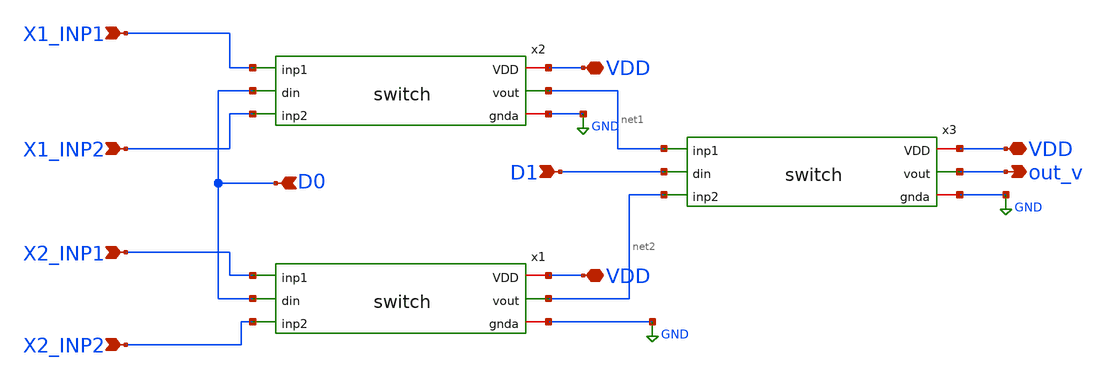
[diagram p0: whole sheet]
** sch_path: week7/pre-layout/untitled-3.sch
**.subckt untitled-3 out_v VDD VDD VDD X1_INP1 X1_INP2 X2_INP1 X2_INP2 D0 D1
*.opin out_v
*.iopin VDD
*.iopin VDD
*.iopin VDD
*.ipin X1_INP1
*.ipin X1_INP2
*.ipin X2_INP1
*.ipin X2_INP2
*.ipin D0
*.ipin D1
x1 X2_INP1 VDD D0 net2 GND X2_INP2 switch
x2 X1_INP1 VDD D0 net1 GND X1_INP2 switch
x3 net1 VDD D1 out_v GND net2 switch
**.ends

* expanding   symbol:  switch.sym # of pins=6
** sym_path: week7/pre-layout/switch.sym
** sch_path: week7/pre-layout/switch.sch
.subckt switch inp1 VDD din vout gnda inp2
*.ipin din
*.iopin VDD
*.ipin inp1
*.ipin inp2
*.iopin gnda
*.opin vout
XM1 net1 din gnda gnda sky130_fd_pr__nfet_01v8 L=0.15 W=0.6 nf=1 ad='int((nf+1)/2) * W/nf * 0.29' as='int((nf+2)/2) * W/nf * 0.29'
+ pd='2*int((nf+1)/2) * (W/nf + 0.29)' ps='2*int((nf+2)/2) * (W/nf + 0.29)' nrd='0.29 / W' nrs='0.29 / W'
+ sa=0 sb=0 sd=0 mult=1 m=1
XM2 net1 din VDD VDD sky130_fd_pr__pfet_01v8 L=0.15 W=1.2 nf=1 ad='int((nf+1)/2) * W/nf * 0.29' as='int((nf+2)/2) * W/nf * 0.29'
+ pd='2*int((nf+1)/2) * (W/nf + 0.29)' ps='2*int((nf+2)/2) * (W/nf + 0.29)' nrd='0.29 / W' nrs='0.29 / W'
+ sa=0 sb=0 sd=0 mult=1 m=1
XM3 net2 net1 VDD VDD sky130_fd_pr__pfet_01v8 L=0.15 W=1.2 nf=1 ad='int((nf+1)/2) * W/nf * 0.29' as='int((nf+2)/2) * W/nf * 0.29'
+ pd='2*int((nf+1)/2) * (W/nf + 0.29)' ps='2*int((nf+2)/2) * (W/nf + 0.29)' nrd='0.29 / W' nrs='0.29 / W'
+ sa=0 sb=0 sd=0 mult=1 m=1
XM4 net2 net1 gnda gnda sky130_fd_pr__nfet_01v8 L=0.15 W=0.6 nf=1 ad='int((nf+1)/2) * W/nf * 0.29' as='int((nf+2)/2) * W/nf * 0.29'
+ pd='2*int((nf+1)/2) * (W/nf + 0.29)' ps='2*int((nf+2)/2) * (W/nf + 0.29)' nrd='0.29 / W' nrs='0.29 / W'
+ sa=0 sb=0 sd=0 mult=1 m=1
XM5 inp2 net2 vout VDD sky130_fd_pr__pfet_01v8 L=0.15 W=1.2 nf=1 ad='int((nf+1)/2) * W/nf * 0.29' as='int((nf+2)/2) * W/nf * 0.29'
+ pd='2*int((nf+1)/2) * (W/nf + 0.29)' ps='2*int((nf+2)/2) * (W/nf + 0.29)' nrd='0.29 / W' nrs='0.29 / W'
+ sa=0 sb=0 sd=0 mult=1 m=1
XM6 inp1 net2 vout GND sky130_fd_pr__nfet_01v8 L=0.15 W=0.6 nf=1 ad='int((nf+1)/2) * W/nf * 0.29' as='int((nf+2)/2) * W/nf * 0.29'
+ pd='2*int((nf+1)/2) * (W/nf + 0.29)' ps='2*int((nf+2)/2) * (W/nf + 0.29)' nrd='0.29 / W' nrs='0.29 / W'
+ sa=0 sb=0 sd=0 mult=1 m=1
XM7 vout net1 inp2 GND sky130_fd_pr__nfet_01v8 L=0.15 W=0.6 nf=1 ad='int((nf+1)/2) * W/nf * 0.29' as='int((nf+2)/2) * W/nf * 0.29'
+ pd='2*int((nf+1)/2) * (W/nf + 0.29)' ps='2*int((nf+2)/2) * (W/nf + 0.29)' nrd='0.29 / W' nrs='0.29 / W'
+ sa=0 sb=0 sd=0 mult=1 m=1
XM8 vout net1 inp1 VDD sky130_fd_pr__pfet_01v8 L=0.15 W=1.2 nf=1 ad='int((nf+1)/2) * W/nf * 0.29' as='int((nf+2)/2) * W/nf * 0.29'
+ pd='2*int((nf+1)/2) * (W/nf + 0.29)' ps='2*int((nf+2)/2) * (W/nf + 0.29)' nrd='0.29 / W' nrs='0.29 / W'
+ sa=0 sb=0 sd=0 mult=1 m=1
.ends

.GLOBAL GND
.end
